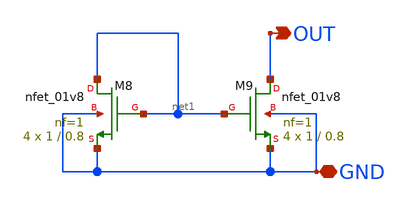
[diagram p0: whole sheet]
** sch_path: opamp1stage/magic/untitled.sch
**.subckt untitled GND OUT
*.iopin GND
*.opin OUT
XM8 net1 net1 GND GND sky130_fd_pr__nfet_01v8 L=0.8 W=1 nf=1 ad='int((nf+1)/2) * W/nf * 0.29' as='int((nf+2)/2) * W/nf * 0.29'
+ pd='2*int((nf+1)/2) * (W/nf + 0.29)' ps='2*int((nf+2)/2) * (W/nf + 0.29)' nrd='0.29 / W' nrs='0.29 / W'
+ sa=0 sb=0 sd=0 mult=4 m=4
XM9 OUT net1 GND GND sky130_fd_pr__nfet_01v8 L=0.8 W=1 nf=1 ad='int((nf+1)/2) * W/nf * 0.29' as='int((nf+2)/2) * W/nf * 0.29'
+ pd='2*int((nf+1)/2) * (W/nf + 0.29)' ps='2*int((nf+2)/2) * (W/nf + 0.29)' nrd='0.29 / W' nrs='0.29 / W'
+ sa=0 sb=0 sd=0 mult=4 m=4
**.ends
.end
